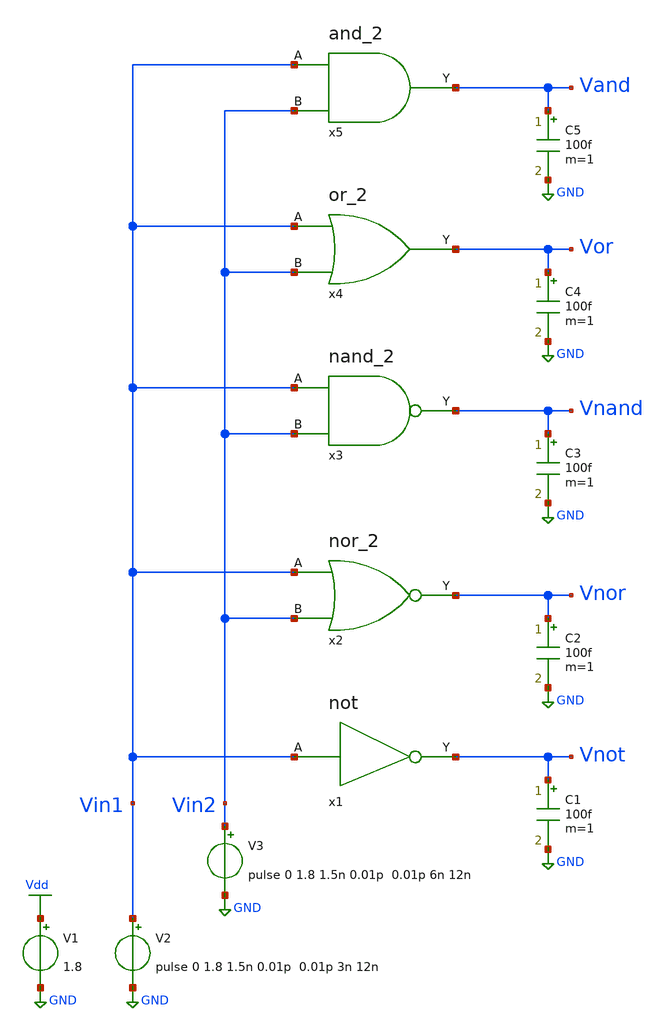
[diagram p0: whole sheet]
** sch_path: Circuiti/logic-gates.sch
**.subckt logic-gates
V1 Vdd GND 1.8
V2 Vin1 GND pulse 0 1.8 1.5n 0.01p 0.01p 3n 12n
V3 Vin2 GND pulse 0 1.8 1.5n 0.01p 0.01p 6n 12n
x1 Vin1 Vnot not
x2 Vin1 Vnor Vin2 nor_2
x3 Vin1 Vnand Vin2 nand_2
x4 Vin1 Vor Vin2 or_2
x5 Vin1 Vand Vin2 and_2
C1 Vnot GND 100f m=1
C2 Vnor GND 100f m=1
C3 Vnand GND 100f m=1
C4 Vor GND 100f m=1
C5 Vand GND 100f m=1
**** begin user architecture code


.lib /home/matteo/xschem_downloads/skywater-pdk/libraries/sky130_fd_pr_ngspice/latest/models/sky130.lib.spice tt

*.include /home/matteo/xschem_downloads/skywater-pdk/libraries/sky130_fd_pr_ngspice/latest/cells/nfet_01v8/sky130_fd_pr__nfet_01v8__tt.corner.spice

.param mc_mm_switch=0
.param mc_pr_switch=1


 .control
tran 0.05n 18n
plot vin1 vin2+2 vnot+4 vnor+6 vnand+8 vor+10 vnand+12
wrdata output.txt vin1 vin2+2 vnot+4 vnor+6 vnand+8 vor+10 vnand+1
.endc

**** end user architecture code
**.ends

* expanding   symbol:  /home/matteo/Documenti/tesi/Circuiti/logic_gates_sch_sym/not.sym # of pins=2
** sym_path: Circuiti/logic_gates_sch_sym/not.sym
** sch_path: Circuiti/logic_gates_sch_sym/not.sch
.subckt not A Y
*.ipin A
*.opin Y
XM1 Y A GND GND sky130_fd_pr__nfet_01v8 L=0.45 W=1 nf=1 ad='int((nf+1)/2) * W/nf * 0.29' as='int((nf+2)/2) * W/nf * 0.29'
+ pd='2*int((nf+1)/2) * (W/nf + 0.29)' ps='2*int((nf+2)/2) * (W/nf + 0.29)' nrd='0.29 / W' nrs='0.29 / W'
+ sa=0 sb=0 sd=0 mult=1 m=1
XM2 Y A Vdd VDD sky130_fd_pr__pfet_01v8 L=0.45 W=4.8 nf=1 ad='int((nf+1)/2) * W/nf * 0.29' as='int((nf+2)/2) * W/nf * 0.29'
+ pd='2*int((nf+1)/2) * (W/nf + 0.29)' ps='2*int((nf+2)/2) * (W/nf + 0.29)' nrd='0.29 / W' nrs='0.29 / W'
+ sa=0 sb=0 sd=0 mult=1 m=1
.ends


* expanding   symbol:  /home/matteo/Documenti/tesi/Circuiti/logic_gates_sch_sym/nor_2.sym # of
*+ pins=3
** sym_path: Circuiti/logic_gates_sch_sym/nor_2.sym
** sch_path: Circuiti/logic_gates_sch_sym/nor_2.sch
.subckt nor_2 A Y B
*.opin Y
*.ipin A
*.ipin B
XM1 Y B GND GND sky130_fd_pr__nfet_01v8 L=0.45 W=1 nf=1 ad='int((nf+1)/2) * W/nf * 0.29' as='int((nf+2)/2) * W/nf * 0.29'
+ pd='2*int((nf+1)/2) * (W/nf + 0.29)' ps='2*int((nf+2)/2) * (W/nf + 0.29)' nrd='0.29 / W' nrs='0.29 / W'
+ sa=0 sb=0 sd=0 mult=1 m=1
XM3 Y B net1 VDD sky130_fd_pr__pfet_01v8 L=0.15 W=4.8 nf=1 ad='int((nf+1)/2) * W/nf * 0.29' as='int((nf+2)/2) * W/nf * 0.29'
+ pd='2*int((nf+1)/2) * (W/nf + 0.29)' ps='2*int((nf+2)/2) * (W/nf + 0.29)' nrd='0.29 / W' nrs='0.29 / W'
+ sa=0 sb=0 sd=0 mult=1 m=1
XM4 net1 A Vdd VDD sky130_fd_pr__pfet_01v8 L=0.15 W=4.8 nf=1 ad='int((nf+1)/2) * W/nf * 0.29' as='int((nf+2)/2) * W/nf * 0.29'
+ pd='2*int((nf+1)/2) * (W/nf + 0.29)' ps='2*int((nf+2)/2) * (W/nf + 0.29)' nrd='0.29 / W' nrs='0.29 / W'
+ sa=0 sb=0 sd=0 mult=1 m=1
XM2 Y A GND GND sky130_fd_pr__nfet_01v8 L=0.45 W=1 nf=1 ad='int((nf+1)/2) * W/nf * 0.29' as='int((nf+2)/2) * W/nf * 0.29'
+ pd='2*int((nf+1)/2) * (W/nf + 0.29)' ps='2*int((nf+2)/2) * (W/nf + 0.29)' nrd='0.29 / W' nrs='0.29 / W'
+ sa=0 sb=0 sd=0 mult=1 m=1
.ends


* expanding   symbol:  /home/matteo/Documenti/tesi/Circuiti/logic_gates_sch_sym/nand_2.sym # of
*+ pins=3
** sym_path: Circuiti/logic_gates_sch_sym/nand_2.sym
** sch_path: Circuiti/logic_gates_sch_sym/nand_2.sch
.subckt nand_2 A Y B
*.ipin A
*.ipin B
*.opin Y
XM1 Y A net1 GND sky130_fd_pr__nfet_01v8 L=0.15 W=1 nf=1 ad='int((nf+1)/2) * W/nf * 0.29' as='int((nf+2)/2) * W/nf * 0.29'
+ pd='2*int((nf+1)/2) * (W/nf + 0.29)' ps='2*int((nf+2)/2) * (W/nf + 0.29)' nrd='0.29 / W' nrs='0.29 / W'
+ sa=0 sb=0 sd=0 mult=1 m=1
XM3 Y B Vdd VDD sky130_fd_pr__pfet_01v8 L=0.45 W=4.8 nf=1 ad='int((nf+1)/2) * W/nf * 0.29' as='int((nf+2)/2) * W/nf * 0.29'
+ pd='2*int((nf+1)/2) * (W/nf + 0.29)' ps='2*int((nf+2)/2) * (W/nf + 0.29)' nrd='0.29 / W' nrs='0.29 / W'
+ sa=0 sb=0 sd=0 mult=1 m=1
XM4 Y A Vdd VDD sky130_fd_pr__pfet_01v8 L=0.45 W=4.8 nf=1 ad='int((nf+1)/2) * W/nf * 0.29' as='int((nf+2)/2) * W/nf * 0.29'
+ pd='2*int((nf+1)/2) * (W/nf + 0.29)' ps='2*int((nf+2)/2) * (W/nf + 0.29)' nrd='0.29 / W' nrs='0.29 / W'
+ sa=0 sb=0 sd=0 mult=1 m=1
XM2 net1 B GND GND sky130_fd_pr__nfet_01v8 L=0.15 W=1 nf=1 ad='int((nf+1)/2) * W/nf * 0.29' as='int((nf+2)/2) * W/nf * 0.29'
+ pd='2*int((nf+1)/2) * (W/nf + 0.29)' ps='2*int((nf+2)/2) * (W/nf + 0.29)' nrd='0.29 / W' nrs='0.29 / W'
+ sa=0 sb=0 sd=0 mult=1 m=1
.ends


* expanding   symbol:  /home/matteo/Documenti/tesi/Circuiti/logic_gates_sch_sym/or_2.sym # of pins=3
** sym_path: Circuiti/logic_gates_sch_sym/or_2.sym
** sch_path: Circuiti/logic_gates_sch_sym/or_2.sch
.subckt or_2 A Y B
*.ipin A
*.ipin B
*.opin Y
x1 A net1 B nor_2
x2 net1 Y not
.ends


* expanding   symbol:  /home/matteo/Documenti/tesi/Circuiti/logic_gates_sch_sym/and_2.sym # of
*+ pins=3
** sym_path: Circuiti/logic_gates_sch_sym/and_2.sym
** sch_path: Circuiti/logic_gates_sch_sym/and_2.sch
.subckt and_2 A Y B
*.ipin B
*.ipin A
*.opin Y
x1 A net1 B nand_2
x2 net1 Y not
.ends

.GLOBAL GND
.GLOBAL Vdd
.end
